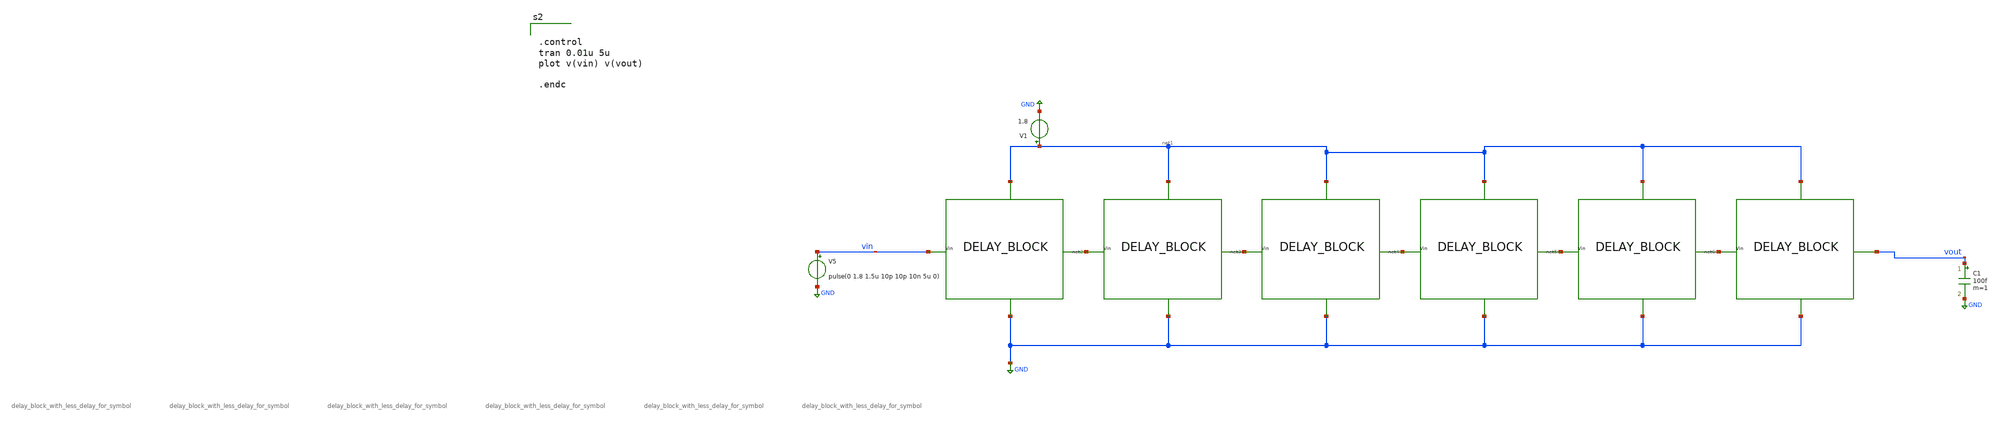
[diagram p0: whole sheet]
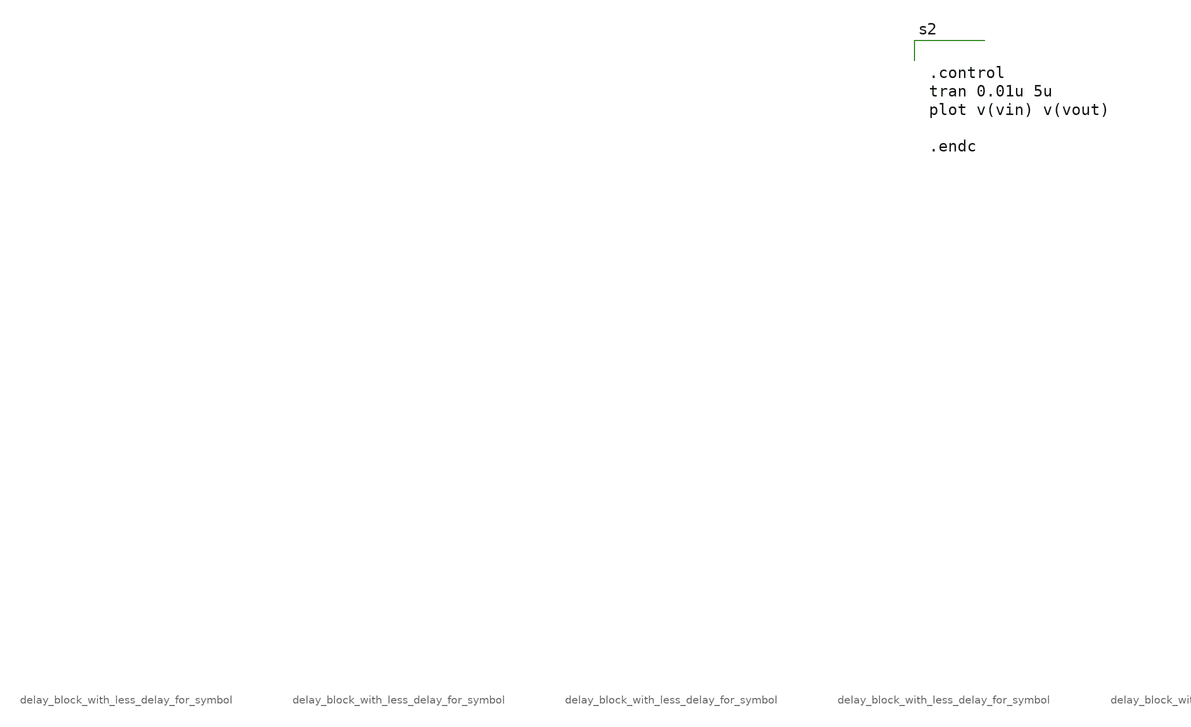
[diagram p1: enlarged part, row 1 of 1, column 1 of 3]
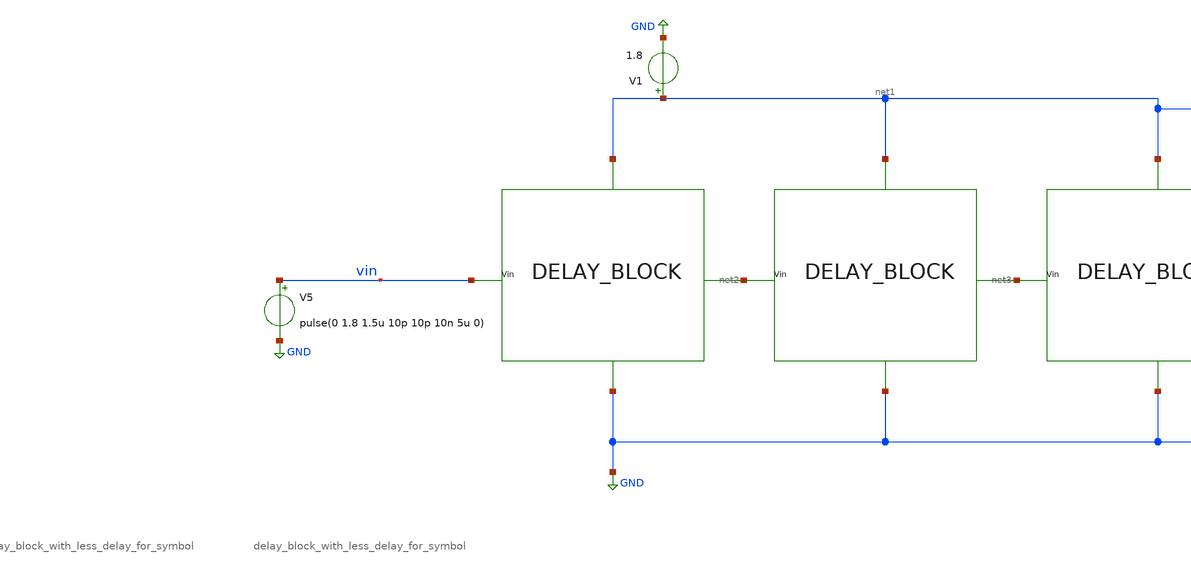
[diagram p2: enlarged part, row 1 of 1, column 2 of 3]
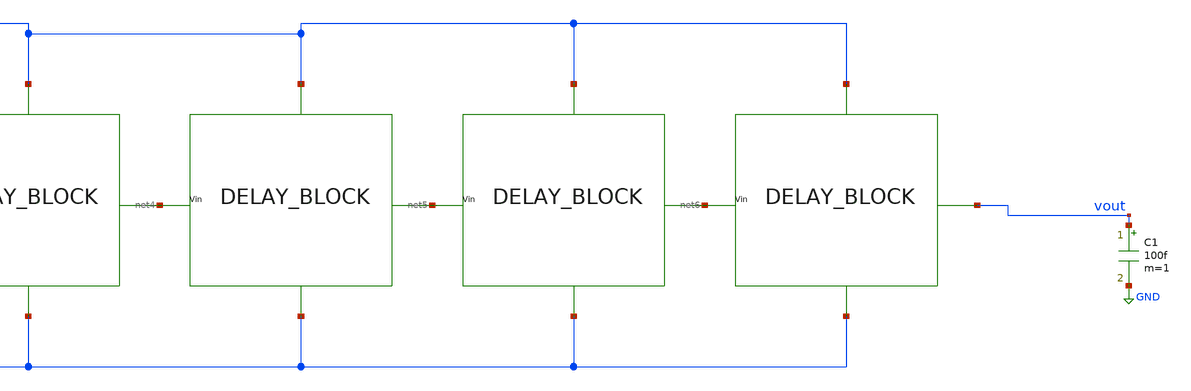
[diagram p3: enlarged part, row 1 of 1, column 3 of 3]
** sch_path: xschem/DC_DC_Converter_xschem/DC_DC_Converter/Delay_block_revised/delay_bpock_tb.sch
**.subckt delay_bpock_tb
V5 vin GND pulse(0 1.8 1.5u 10p 10p 10n 5u 0)
C1 vout GND 100f m=1
X1 vin net2 net1 GND delay_block_with_less_delay_for_symbol
X2 net2 net3 net1 GND delay_block_with_less_delay_for_symbol
X3 net3 net4 net1 GND delay_block_with_less_delay_for_symbol
X4 net4 net5 net1 GND delay_block_with_less_delay_for_symbol
X5 net5 net6 net1 GND delay_block_with_less_delay_for_symbol
X6 net6 vout net1 GND delay_block_with_less_delay_for_symbol
V1 net1 GND 1.8
**** begin user architecture code


.control
tran 0.01u 5u
plot v(vin) v(vout)

.endc



** opencircuitdesign pdks install
.lib $::SKYWATER_MODELS/sky130.lib.spice tt


**** end user architecture code
**.ends
.GLOBAL GND
.end
